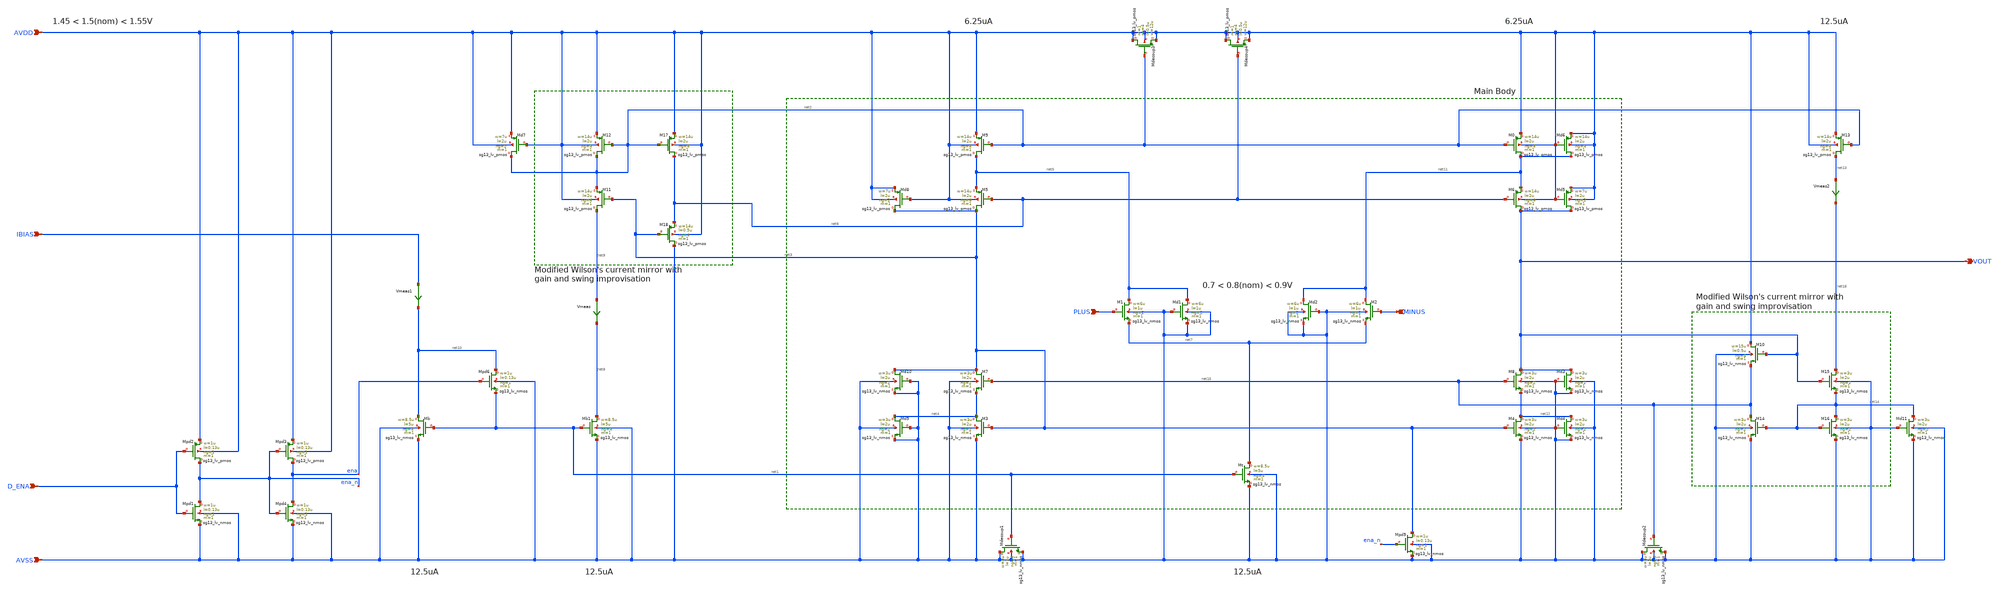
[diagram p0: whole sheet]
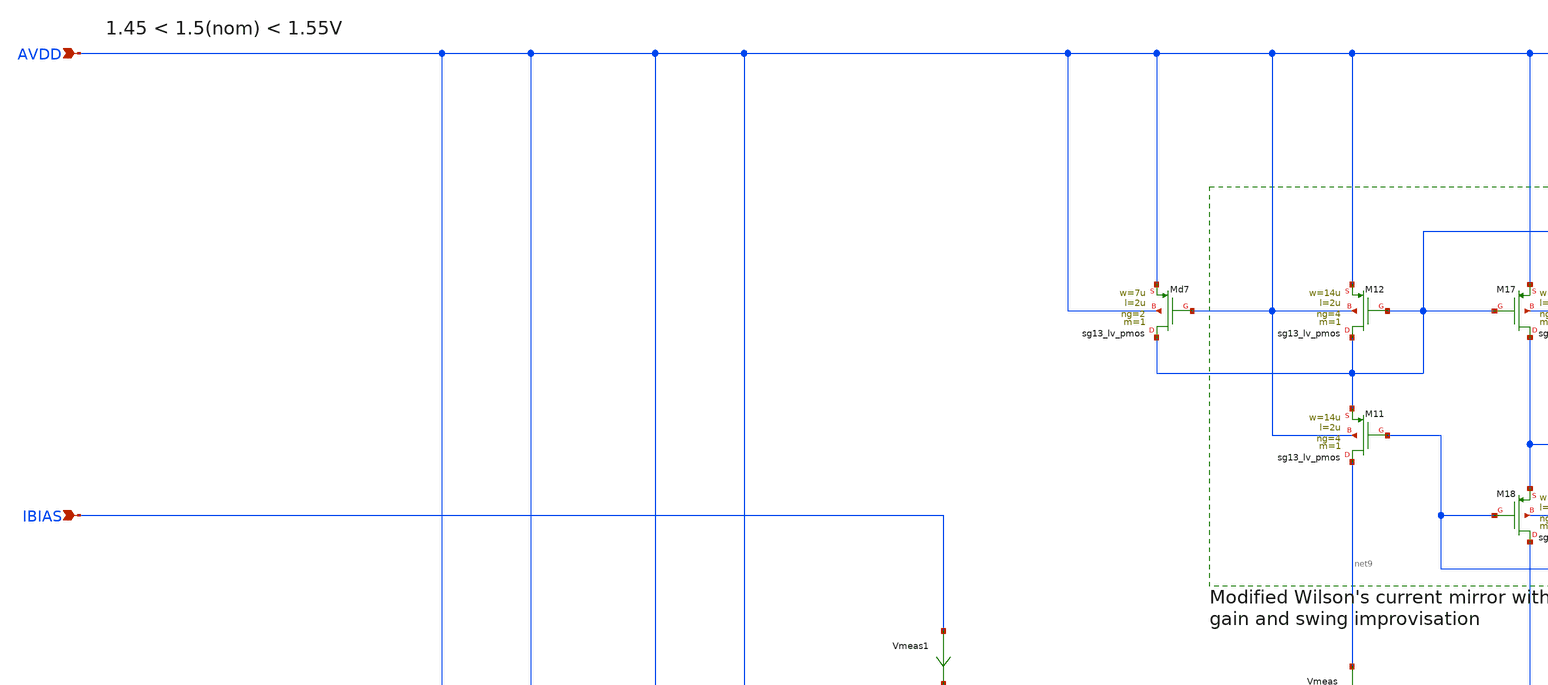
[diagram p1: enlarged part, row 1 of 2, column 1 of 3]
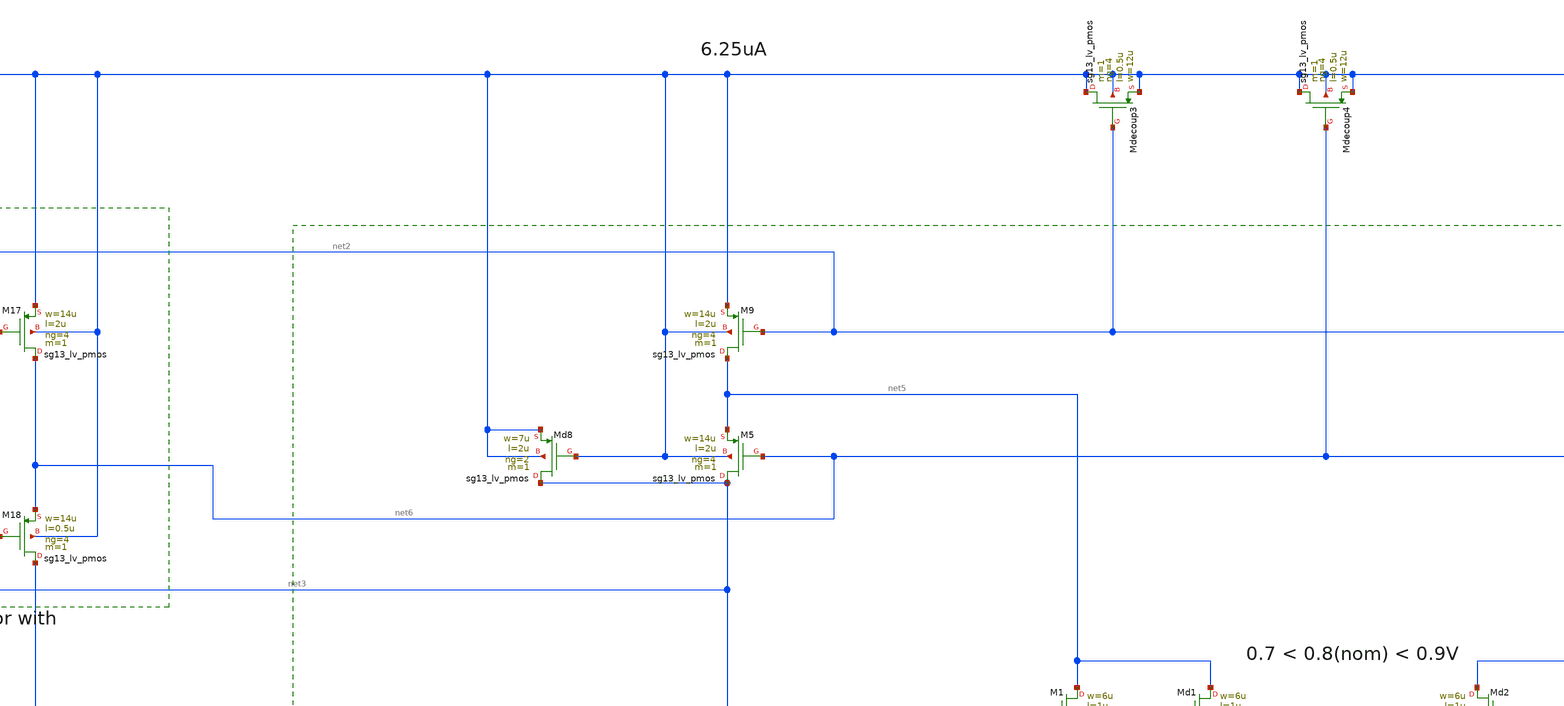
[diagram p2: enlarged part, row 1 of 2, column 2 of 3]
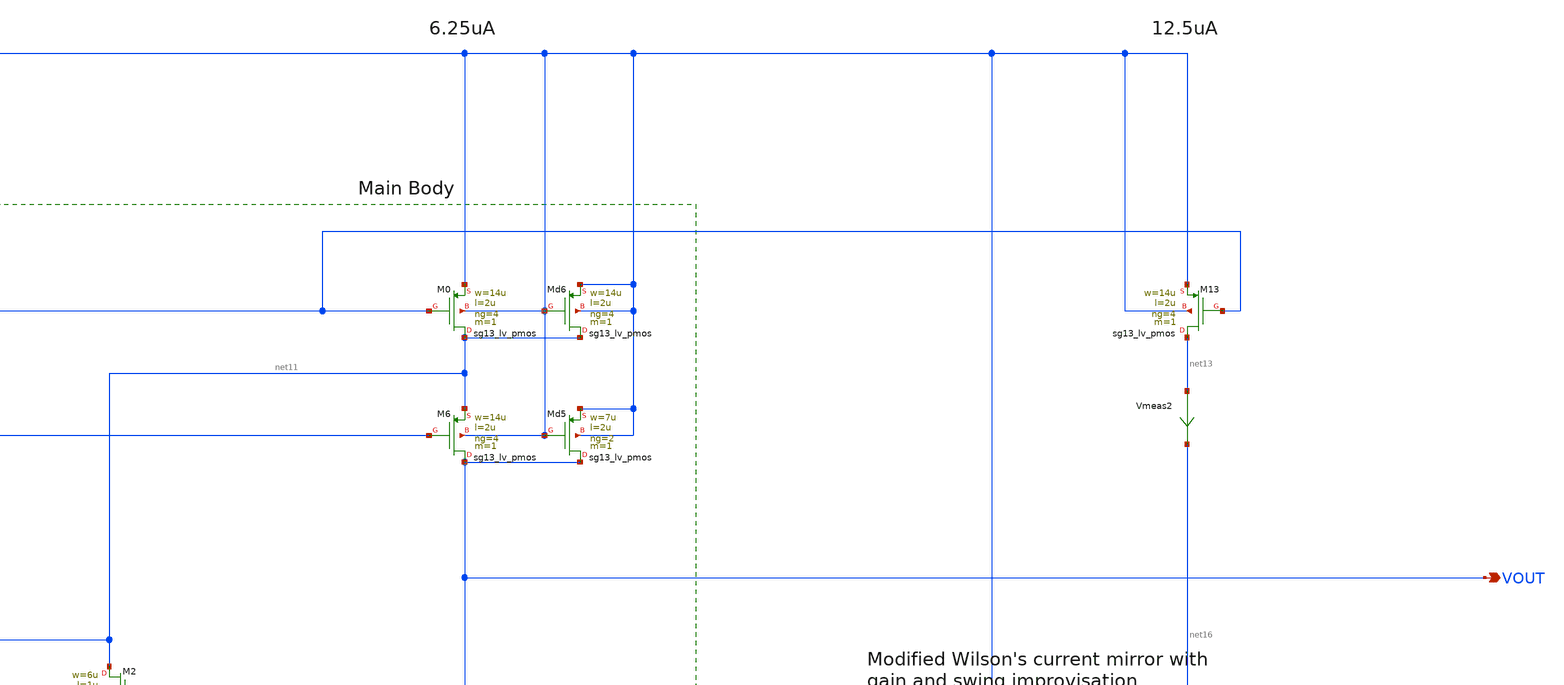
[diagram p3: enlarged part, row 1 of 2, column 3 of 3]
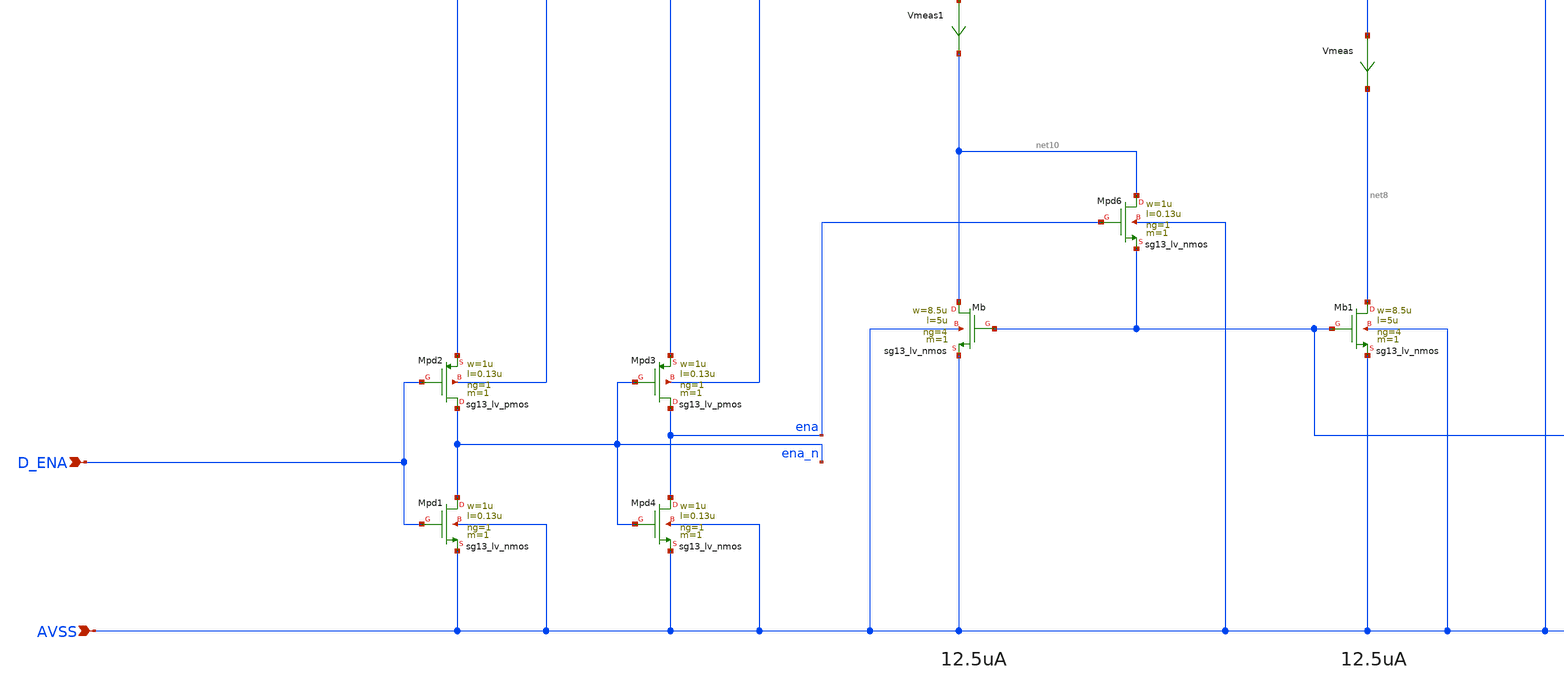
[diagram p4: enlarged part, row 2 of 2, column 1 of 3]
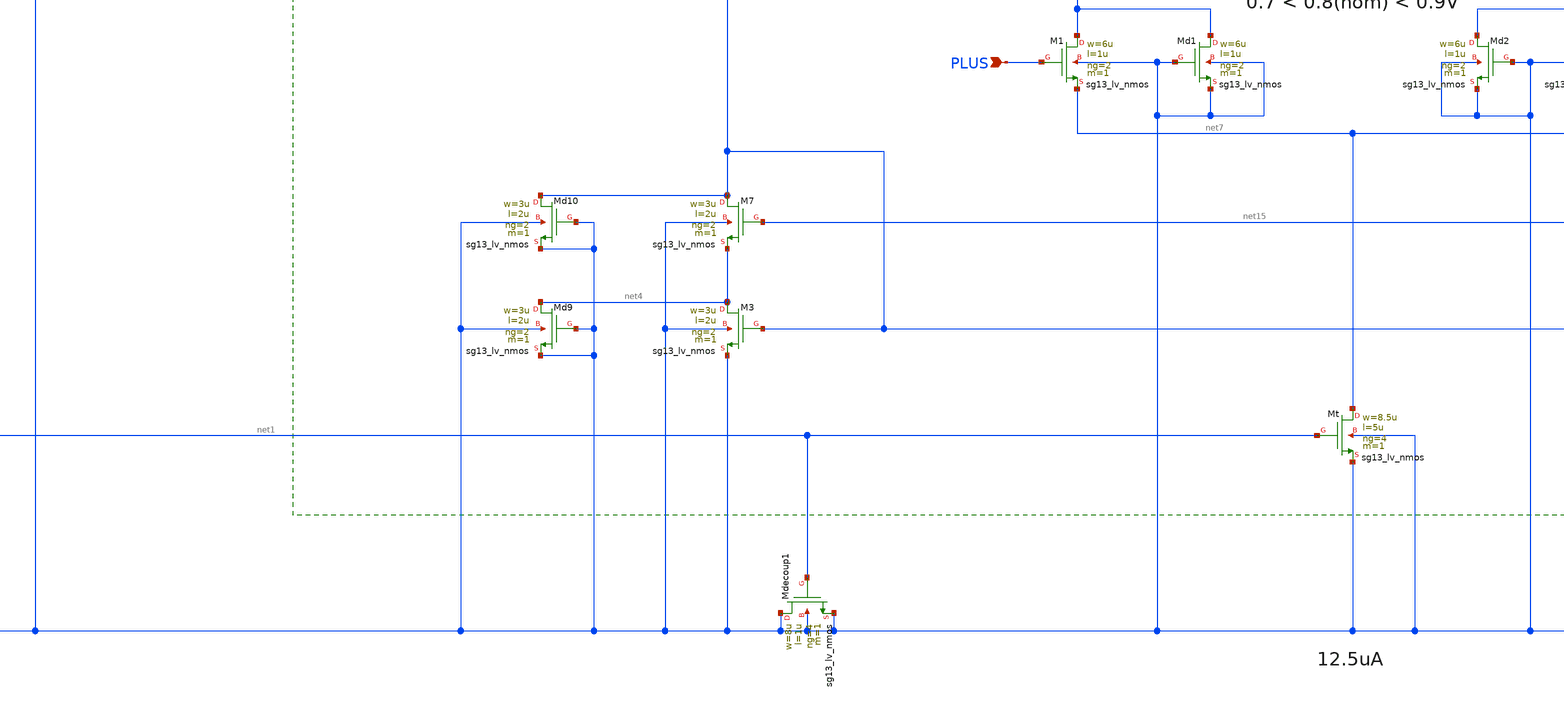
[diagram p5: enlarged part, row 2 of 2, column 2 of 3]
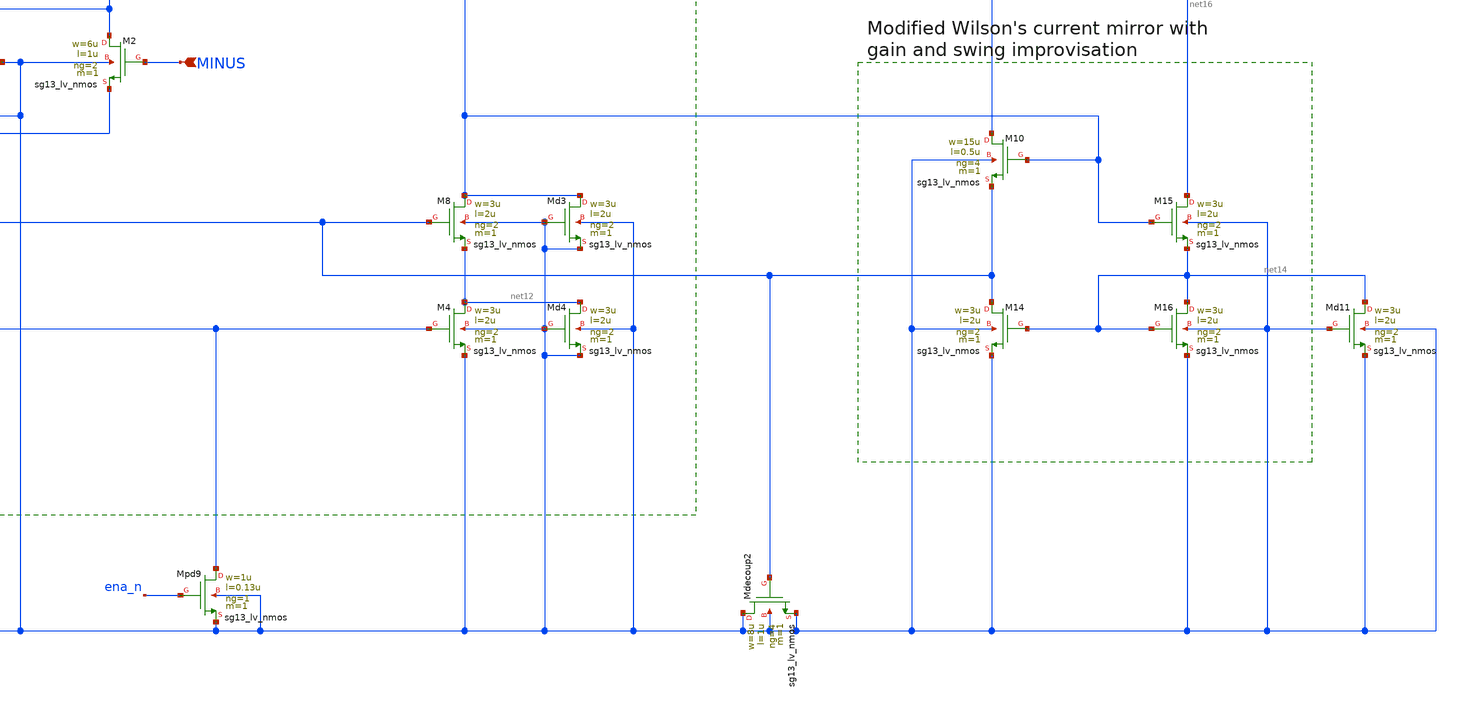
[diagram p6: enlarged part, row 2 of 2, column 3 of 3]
** sch_path: Designs/otas/1_schematics/foldedcascode_nmos_withdummies.sch
* (c) 2025 Thesis_HP, Apache-2.0 license
**.subckt foldedcascode_nmos_withdummies AVSS IBIAS AVDD PLUS MINUS VOUT D_ENA
*.ipin AVSS
*.ipin IBIAS
*.ipin AVDD
*.ipin PLUS
*.ipin MINUS
*.opin VOUT
*.ipin D_ENA
XMb net10 net1 AVSS AVSS sg13_lv_nmos w=8.5u l=5u ng=4 m=1 mm_ok=1
XMpd6 net10 ena net1 AVSS sg13_lv_nmos w=1u l=0.13u ng=1 m=1 mm_ok=1
XMb1 net8 net1 AVSS AVSS sg13_lv_nmos w=8.5u l=5u ng=4 m=1 mm_ok=1
Vmeas net9 net8 0
.save i(vmeas)
XM11 net9 net3 net2 AVDD sg13_lv_pmos w=14u l=2u ng=4 m=1 mm_ok=1
XM12 net2 net2 AVDD AVDD sg13_lv_pmos w=14u l=2u ng=4 m=1 mm_ok=1
XM18 AVSS net3 net6 AVDD sg13_lv_pmos w=14u l=0.5u ng=4 m=1 mm_ok=1
XM17 net6 net2 AVDD AVDD sg13_lv_pmos w=14u l=2u ng=4 m=1 mm_ok=1
XM9 net5 net2 AVDD AVDD sg13_lv_pmos w=14u l=2u ng=4 m=1 mm_ok=1
XM5 net3 net6 net5 AVDD sg13_lv_pmos w=14u l=2u ng=4 m=1 mm_ok=1
XM7 net3 net15 net4 AVSS sg13_lv_nmos w=3u l=2u ng=2 m=1 mm_ok=1
XM3 net4 net3 AVSS AVSS sg13_lv_nmos w=3u l=2u ng=2 m=1 mm_ok=1
XMt net7 net1 AVSS AVSS sg13_lv_nmos w=8.5u l=5u ng=4 m=1 mm_ok=1
XM1 net5 PLUS net7 AVSS sg13_lv_nmos w=6u l=1u ng=2 m=1 mm_ok=1
XM2 net11 MINUS net7 AVSS sg13_lv_nmos w=6u l=1u ng=2 m=1 mm_ok=1
XMdecoup3 AVDD net2 AVDD AVDD sg13_lv_pmos w=12u l=0.5u ng=4 m=1 mm_ok=1
XMdecoup4 AVDD net6 AVDD AVDD sg13_lv_pmos w=12u l=0.5u ng=4 m=1 mm_ok=1
XMdecoup1 AVSS net1 AVSS AVSS sg13_lv_nmos w=8u l=1u ng=4 m=1 mm_ok=1
XMpd2 ena_n D_ENA AVDD AVDD sg13_lv_pmos w=1u l=0.13u ng=1 m=1 mm_ok=1
Vmeas1 IBIAS net10 0
.save i(vmeas1)
XMpd3 ena ena_n AVDD AVDD sg13_lv_pmos w=1u l=0.13u ng=1 m=1 mm_ok=1
XMpd1 ena_n D_ENA AVSS AVSS sg13_lv_nmos w=1u l=0.13u ng=1 m=1 mm_ok=1
XMpd4 ena ena_n AVSS AVSS sg13_lv_nmos w=1u l=0.13u ng=1 m=1 mm_ok=1
XMd2 net11 AVSS AVSS AVSS sg13_lv_nmos w=6u l=1u ng=2 m=1 mm_ok=1
XM6 VOUT net6 net11 AVDD sg13_lv_pmos w=14u l=2u ng=4 m=1 mm_ok=1
XM0 net11 net2 AVDD AVDD sg13_lv_pmos w=14u l=2u ng=4 m=1 mm_ok=1
XM8 VOUT net15 net12 AVSS sg13_lv_nmos w=3u l=2u ng=2 m=1 mm_ok=1
XM4 net12 net3 AVSS AVSS sg13_lv_nmos w=3u l=2u ng=2 m=1 mm_ok=1
XMd4 net12 AVSS AVSS AVSS sg13_lv_nmos w=3u l=2u ng=2 m=1 mm_ok=1
XMd3 VOUT AVSS AVSS AVSS sg13_lv_nmos w=3u l=2u ng=2 m=1 mm_ok=1
XMd6 net11 AVDD AVDD AVDD sg13_lv_pmos w=14u l=2u ng=4 m=1 mm_ok=1
XMd5 VOUT AVDD AVDD AVDD sg13_lv_pmos w=7u l=2u ng=2 m=1 mm_ok=1
XM13 net13 net2 AVDD AVDD sg13_lv_pmos w=14u l=2u ng=4 m=1 mm_ok=1
Vmeas2 net13 net16 0
.save i(vmeas2)
XM15 net16 VOUT net14 AVSS sg13_lv_nmos w=3u l=2u ng=2 m=1 mm_ok=1
XM16 net14 net14 AVSS AVSS sg13_lv_nmos w=3u l=2u ng=2 m=1 mm_ok=1
XM14 net15 net14 AVSS AVSS sg13_lv_nmos w=3u l=2u ng=2 m=1 mm_ok=1
XM10 AVDD VOUT net15 AVSS sg13_lv_nmos w=15u l=0.5u ng=4 m=1 mm_ok=1
XMdecoup2 AVSS net15 AVSS AVSS sg13_lv_nmos w=8u l=1u ng=4 m=1 mm_ok=1
XMpd9 net3 ena_n AVSS AVSS sg13_lv_nmos w=1u l=0.13u ng=1 m=1 mm_ok=1
XMd1 net5 AVSS AVSS AVSS sg13_lv_nmos w=6u l=1u ng=2 m=1 mm_ok=1
XMd8 net3 AVDD AVDD AVDD sg13_lv_pmos w=7u l=2u ng=2 m=1 mm_ok=1
XMd9 net4 AVSS AVSS AVSS sg13_lv_nmos w=3u l=2u ng=2 m=1 mm_ok=1
XMd10 net3 AVSS AVSS AVSS sg13_lv_nmos w=3u l=2u ng=2 m=1 mm_ok=1
XMd7 net2 AVDD AVDD AVDD sg13_lv_pmos w=7u l=2u ng=2 m=1 mm_ok=1
XMd11 net14 AVSS AVSS AVSS sg13_lv_nmos w=3u l=2u ng=2 m=1 mm_ok=1
**.ends
.end
